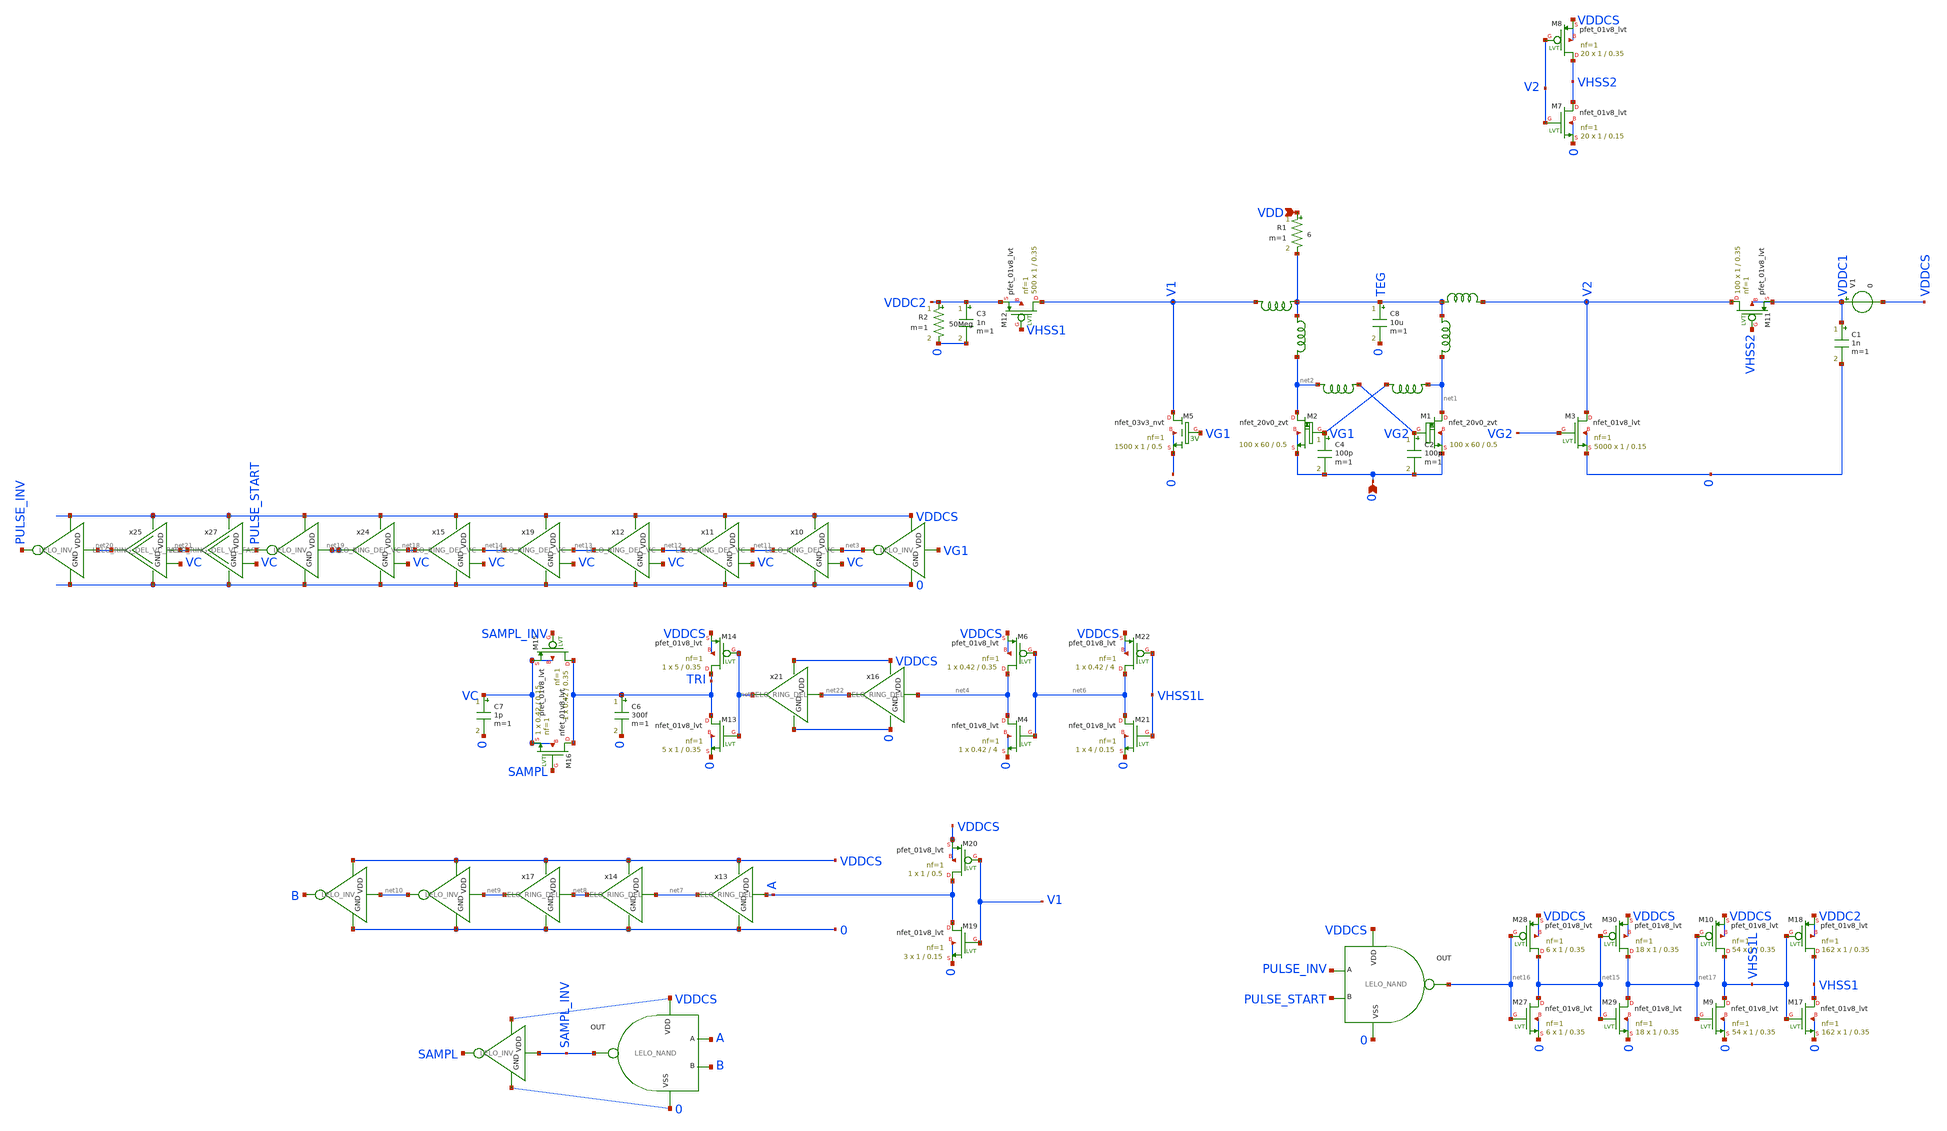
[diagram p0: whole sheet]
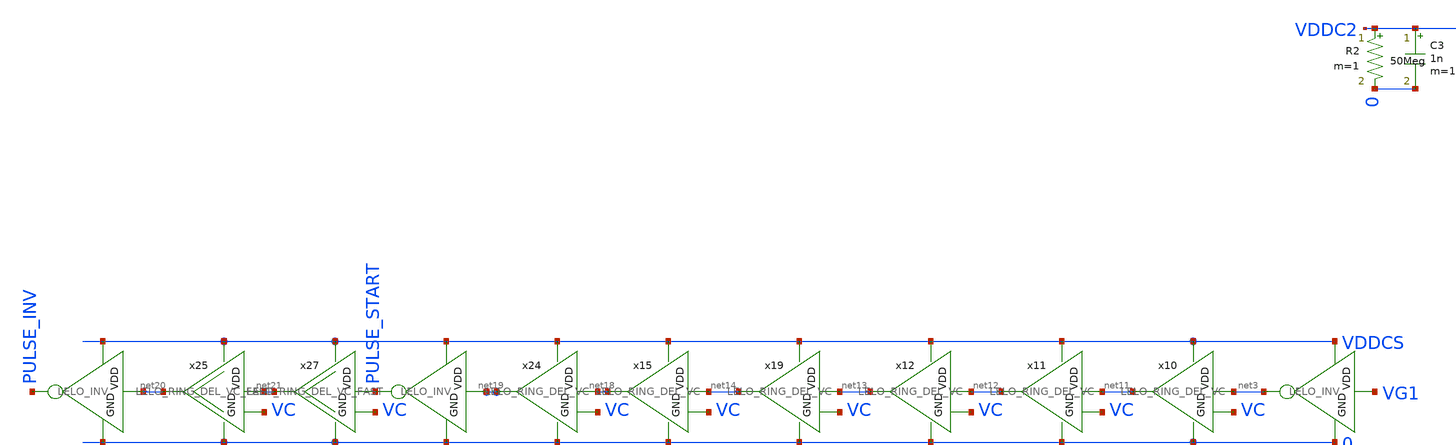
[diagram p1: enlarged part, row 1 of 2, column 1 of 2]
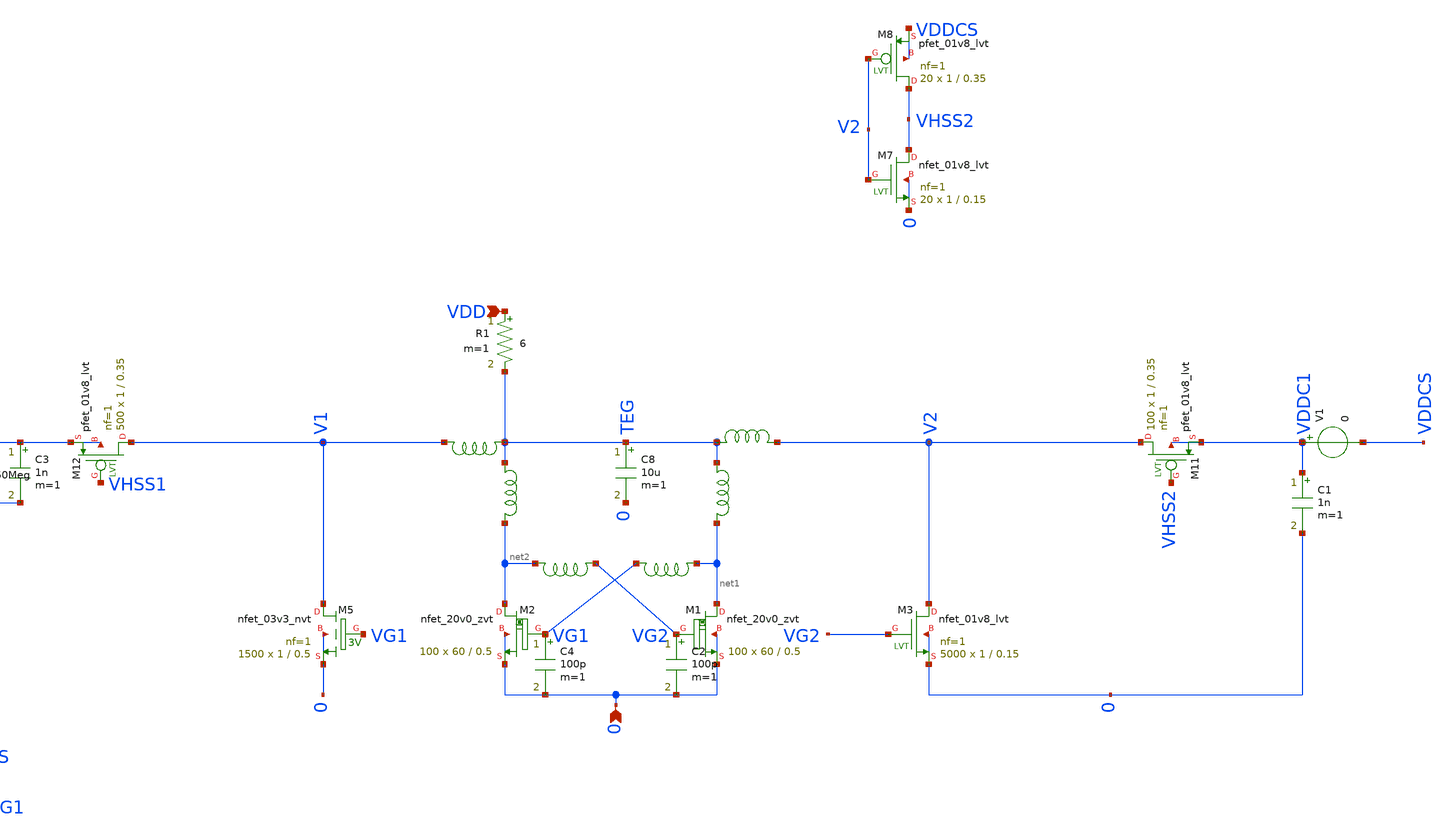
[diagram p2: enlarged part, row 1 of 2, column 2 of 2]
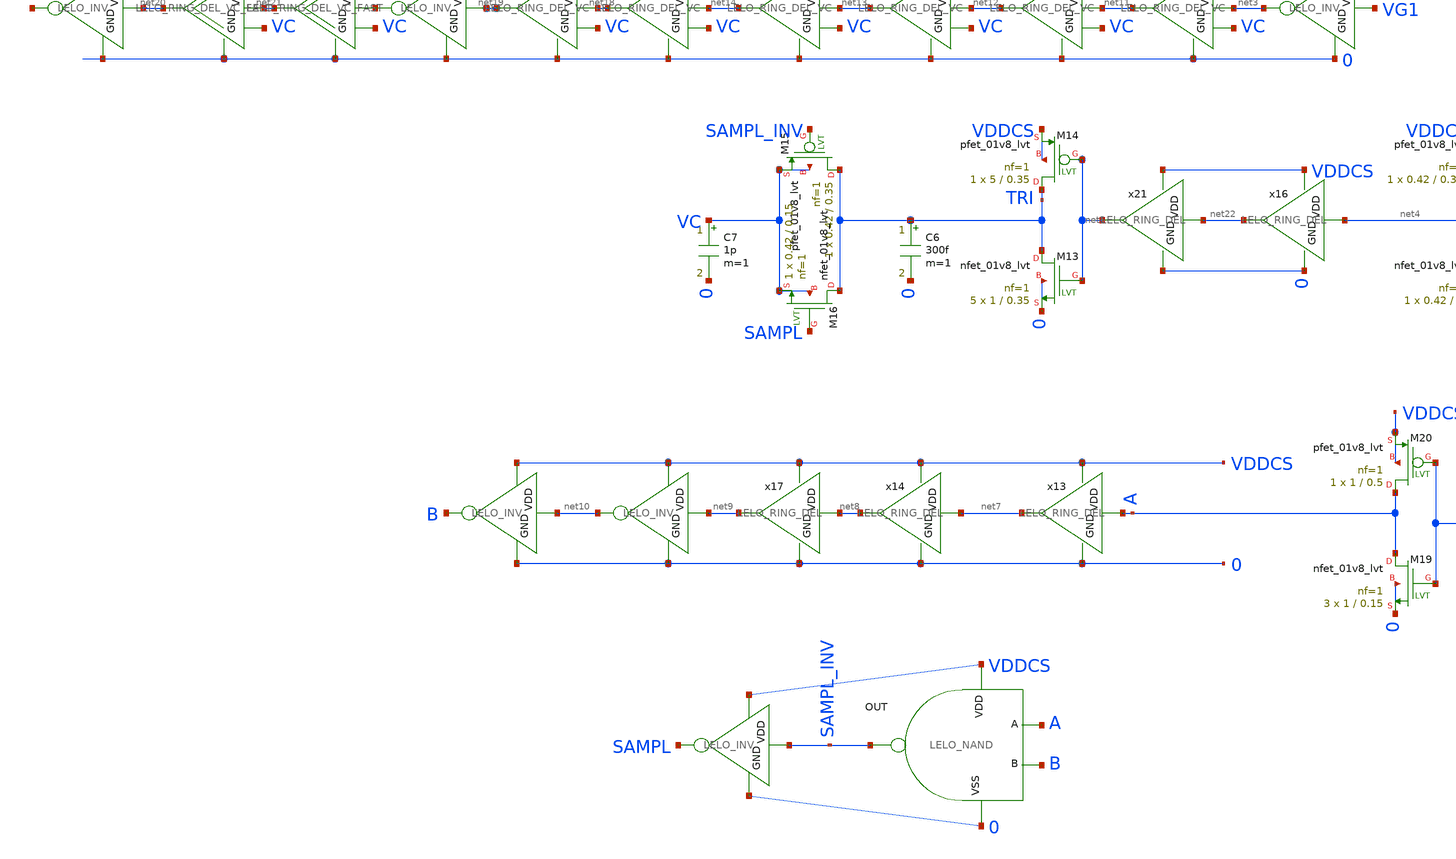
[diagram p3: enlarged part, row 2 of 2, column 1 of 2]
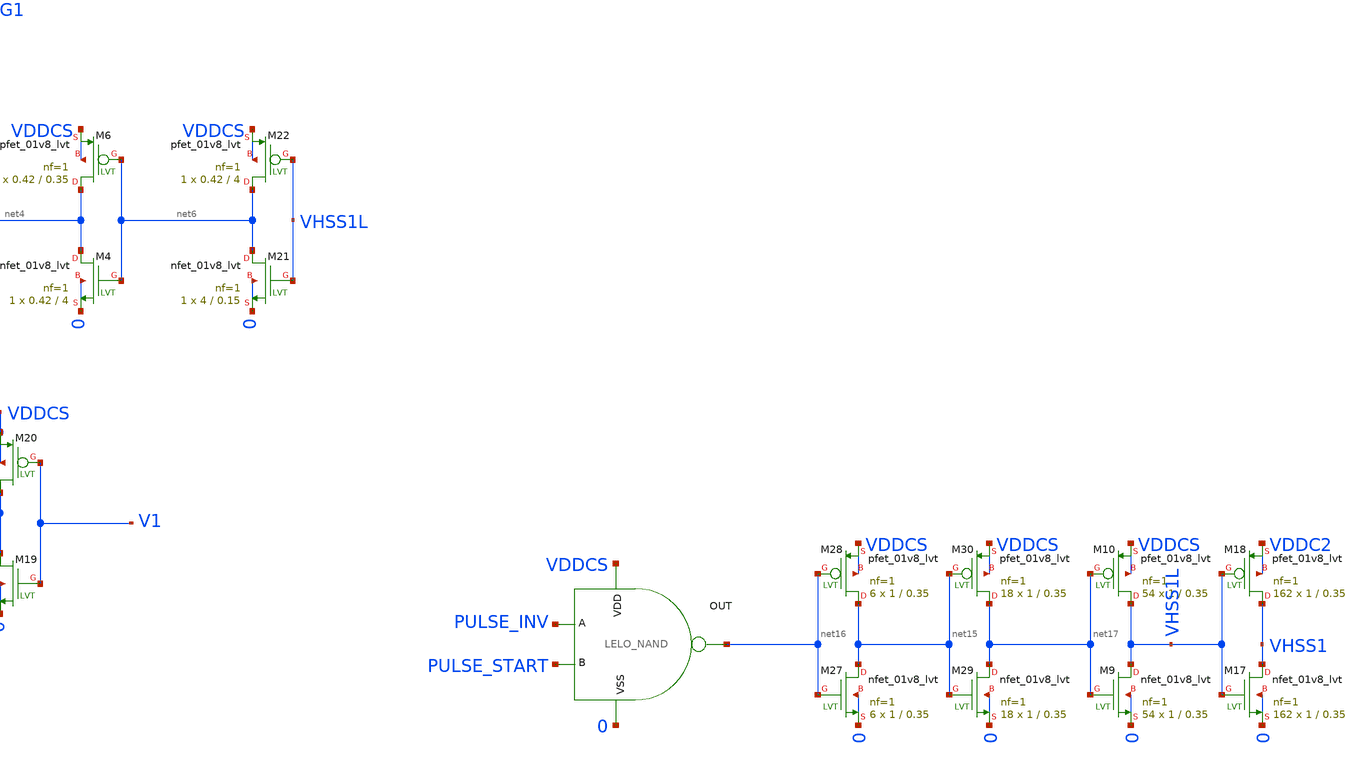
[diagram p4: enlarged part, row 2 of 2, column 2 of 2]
** sch_path: design/LELO_SVOD_SKY130A/LELO_EXSC.sch
**.subckt LELO_EXSC 0 VDD
*.ipin 0
*.ipin VDD
C1 VDDC1 0 1n m=1
C2 VG2 0 100p m=1
R1 VDD TEG 6 m=1
XM3 V2 VG2 0 0 sky130_fd_pr__nfet_01v8_lvt L=0.15 W=1 nf=1 ad='int((1 + 1)/2) * 1 / 1 * 0.29' as='int((1 + 2)/2) * 1 / 1 * 0.29'
+ pd='2*int((1 + 1)/2) * (1 / 1 + 0.29)' ps='2*int((1 + 2)/2) * (1 / 1 + 0.29)' nrd='0.29 / 1 ' nrs='0.29 / 1 '
+ sa=0 sb=0 sd=0 mult=5000 m=5000
x1 VG2 net2 1812PS-564_imp
x2 net1 VG1 1812PS-564_imp
C4 VG1 0 100p m=1
XM11 V2 VHSS2 VDDC1 VDDC1 sky130_fd_pr__pfet_01v8_lvt L=0.35 W=1 nf=1 ad='int((1 + 1)/2) * 1 / 1 * 0.29'
+ as='int((1 + 2)/2) * 1 / 1 * 0.29' pd='2*int((1 + 1)/2) * (1 / 1 + 0.29)' ps='2*int((1 + 2)/2) * (1 / 1 + 0.29)'
+ nrd='0.29 / 1 ' nrs='0.29 / 1 ' sa=0 sb=0 sd=0 mult=100 m=100
XM12 V1 VHSS1 VDDC2 VDDC2 sky130_fd_pr__pfet_01v8_lvt L=0.35 W=1 nf=1 ad='int((1 + 1)/2) * 1 / 1 * 0.29'
+ as='int((1 + 2)/2) * 1 / 1 * 0.29' pd='2*int((1 + 1)/2) * (1 / 1 + 0.29)' ps='2*int((1 + 2)/2) * (1 / 1 + 0.29)'
+ nrd='0.29 / 1 ' nrs='0.29 / 1 ' sa=0 sb=0 sd=0 mult=500 m=500
XM1 net1 VG2 0 0 sky130_fd_pr__nfet_20v0_zvt W=60 L=0.5 m=100
XM2 net2 VG1 0 0 sky130_fd_pr__nfet_20v0_zvt W=60 L=0.5 m=100
x9 VDDCS VG1 net3 0 LELO_INV
XM4 net4 net6 0 0 sky130_fd_pr__nfet_01v8_lvt L=4 W=0.42 nf=1 ad='int((1 + 1)/2) * 0.42 / 1 * 0.29' as='int((1 + 2)/2) * 0.42 / 1 * 0.29'
+ pd='2*int((1 + 1)/2) * (0.42 / 1 + 0.29)' ps='2*int((1 + 2)/2) * (0.42 / 1 + 0.29)' nrd='0.29 / 0.42 '
+ nrs='0.29 / 0.42 ' sa=0 sb=0 sd=0 mult=1 m=1
XM6 net4 net6 VDDCS VDDCS sky130_fd_pr__pfet_01v8_lvt L=0.35 W=0.42 nf=1 ad='int((1 + 1)/2) * 0.42 / 1 * 0.29'
+ as='int((1 + 2)/2) * 0.42 / 1 * 0.29' pd='2*int((1 + 1)/2) * (0.42 / 1 + 0.29)' ps='2*int((1 + 2)/2) * (0.42 / 1 + 0.29)'
+ nrd='0.29 / 0.42 ' nrs='0.29 / 0.42 ' sa=0 sb=0 sd=0 mult=1 m=1
XM13 TRI net5 0 0 sky130_fd_pr__nfet_01v8_lvt L=0.35 W=1 nf=1 ad='int((1 + 1)/2) * 1 / 1 * 0.29' as='int((1 + 2)/2) * 1 / 1 * 0.29'
+ pd='2*int((1 + 1)/2) * (1 / 1 + 0.29)' ps='2*int((1 + 2)/2) * (1 / 1 + 0.29)' nrd='0.29 / 1 ' nrs='0.29 / 1 '
+ sa=0 sb=0 sd=0 mult=5 m=5
XM14 TRI net5 VDDCS VDDCS sky130_fd_pr__pfet_01v8_lvt L=0.35 W=5 nf=1 ad='int((1 + 1)/2) * 5 / 1 * 0.29'
+ as='int((1 + 2)/2) * 5 / 1 * 0.29' pd='2*int((1 + 1)/2) * (5 / 1 + 0.29)' ps='2*int((1 + 2)/2) * (5 / 1 + 0.29)'
+ nrd='0.29 / 5 ' nrs='0.29 / 5 ' sa=0 sb=0 sd=0 mult=1 m=1
C6 TRI 0 300f m=1
C7 VC 0 1p m=1
XM15 TRI SAMPL_INV VC VC sky130_fd_pr__pfet_01v8_lvt L=0.35 W=0.42 nf=1 ad='int((1 + 1)/2) * 0.42 / 1 * 0.29'
+ as='int((1 + 2)/2) * 0.42 / 1 * 0.29' pd='2*int((1 + 1)/2) * (0.42 / 1 + 0.29)' ps='2*int((1 + 2)/2) * (0.42 / 1 + 0.29)'
+ nrd='0.29 / 0.42 ' nrs='0.29 / 0.42 ' sa=0 sb=0 sd=0 mult=1 m=1
XM16 TRI SAMPL VC VC sky130_fd_pr__nfet_01v8_lvt L=0.15 W=0.42 nf=1 ad='int((1 + 1)/2) * 0.42 / 1 * 0.29'
+ as='int((1 + 2)/2) * 0.42 / 1 * 0.29' pd='2*int((1 + 1)/2) * (0.42 / 1 + 0.29)' ps='2*int((1 + 2)/2) * (0.42 / 1 + 0.29)'
+ nrd='0.29 / 0.42 ' nrs='0.29 / 0.42 ' sa=0 sb=0 sd=0 mult=1 m=1
x13 VDDCS A net7 0 LELO_RING_DEL
x14 VDDCS net7 net8 0 LELO_RING_DEL
x10 VDDCS net3 net11 0 VC LELO_RING_DEL_VC
x11 VDDCS net11 net12 0 VC LELO_RING_DEL_VC
x12 VDDCS net12 net13 0 VC LELO_RING_DEL_VC
C8 TEG 0 10u m=1
x20 VDDCS SAMPL_INV A B 0 LELO_NAND
x17 VDDCS net8 net9 0 LELO_RING_DEL
x18 VDDCS net9 net10 0 LELO_INV
x22 VDDCS net10 B 0 LELO_INV
x23 VDDCS SAMPL_INV SAMPL 0 LELO_INV
x19 VDDCS net13 net14 0 VC LELO_RING_DEL_VC
XM19 A V1 0 0 sky130_fd_pr__nfet_01v8_lvt L=0.15 W=1 nf=1 ad='int((1 + 1)/2) * 1 / 1 * 0.29' as='int((1 + 2)/2) * 1 / 1 * 0.29'
+ pd='2*int((1 + 1)/2) * (1 / 1 + 0.29)' ps='2*int((1 + 2)/2) * (1 / 1 + 0.29)' nrd='0.29 / 1 ' nrs='0.29 / 1 '
+ sa=0 sb=0 sd=0 mult=3 m=3
XM20 A V1 VDDCS VDDCS sky130_fd_pr__pfet_01v8_lvt L=0.5 W=1 nf=1 ad='int((1 + 1)/2) * 1 / 1 * 0.29' as='int((1 + 2)/2) * 1 / 1 * 0.29'
+ pd='2*int((1 + 1)/2) * (1 / 1 + 0.29)' ps='2*int((1 + 2)/2) * (1 / 1 + 0.29)' nrd='0.29 / 1 ' nrs='0.29 / 1 '
+ sa=0 sb=0 sd=0 mult=1 m=1
XM7 VHSS2 V2 0 0 sky130_fd_pr__nfet_01v8_lvt L=0.15 W=1 nf=1 ad='int((1 + 1)/2) * 1 / 1 * 0.29' as='int((1 + 2)/2) * 1 / 1 * 0.29'
+ pd='2*int((1 + 1)/2) * (1 / 1 + 0.29)' ps='2*int((1 + 2)/2) * (1 / 1 + 0.29)' nrd='0.29 / 1 ' nrs='0.29 / 1 '
+ sa=0 sb=0 sd=0 mult=20 m=20
XM8 VHSS2 V2 VDDCS VDDCS sky130_fd_pr__pfet_01v8_lvt L=0.35 W=1 nf=1 ad='int((1 + 1)/2) * 1 / 1 * 0.29'
+ as='int((1 + 2)/2) * 1 / 1 * 0.29' pd='2*int((1 + 1)/2) * (1 / 1 + 0.29)' ps='2*int((1 + 2)/2) * (1 / 1 + 0.29)'
+ nrd='0.29 / 1 ' nrs='0.29 / 1 ' sa=0 sb=0 sd=0 mult=20 m=20
x8 VDDCS net16 PULSE_INV PULSE_START 0 LELO_NAND
XM27 net15 net16 0 0 sky130_fd_pr__nfet_01v8_lvt L=0.35 W=1 nf=1 ad='int((1 + 1)/2) * 1 / 1 * 0.29' as='int((1 + 2)/2) * 1 / 1 * 0.29'
+ pd='2*int((1 + 1)/2) * (1 / 1 + 0.29)' ps='2*int((1 + 2)/2) * (1 / 1 + 0.29)' nrd='0.29 / 1 ' nrs='0.29 / 1 '
+ sa=0 sb=0 sd=0 mult=6 m=6
XM28 net15 net16 VDDCS VDDCS sky130_fd_pr__pfet_01v8_lvt L=0.35 W=1 nf=1 ad='int((1 + 1)/2) * 1 / 1 * 0.29'
+ as='int((1 + 2)/2) * 1 / 1 * 0.29' pd='2*int((1 + 1)/2) * (1 / 1 + 0.29)' ps='2*int((1 + 2)/2) * (1 / 1 + 0.29)'
+ nrd='0.29 / 1 ' nrs='0.29 / 1 ' sa=0 sb=0 sd=0 mult=6 m=6
XM29 net17 net15 0 0 sky130_fd_pr__nfet_01v8_lvt L=0.35 W=1 nf=1 ad='int((1 + 1)/2) * 1 / 1 * 0.29' as='int((1 + 2)/2) * 1 / 1 * 0.29'
+ pd='2*int((1 + 1)/2) * (1 / 1 + 0.29)' ps='2*int((1 + 2)/2) * (1 / 1 + 0.29)' nrd='0.29 / 1 ' nrs='0.29 / 1 '
+ sa=0 sb=0 sd=0 mult=18 m=18
XM30 net17 net15 VDDCS VDDCS sky130_fd_pr__pfet_01v8_lvt L=0.35 W=1 nf=1 ad='int((1 + 1)/2) * 1 / 1 * 0.29'
+ as='int((1 + 2)/2) * 1 / 1 * 0.29' pd='2*int((1 + 1)/2) * (1 / 1 + 0.29)' ps='2*int((1 + 2)/2) * (1 / 1 + 0.29)'
+ nrd='0.29 / 1 ' nrs='0.29 / 1 ' sa=0 sb=0 sd=0 mult=18 m=18
x3 TEG net2 1812PS-103_imp
x4 TEG net1 1812PS-103_imp
x5 TEG V2 XGL6030-822_sat
x25 VDDCS net21 net20 0 VC LELO_RING_DEL_VC_FAST
x6 VDDCS net20 PULSE_INV 0 LELO_INV
x15 VDDCS net14 net18 0 VC LELO_RING_DEL_VC
C3 VDDC2 0 1n m=1
R2 VDDC2 0 50Meg m=1
V1 VDDC1 VDDCS 0
.save i(v1)
XM9 VHSS1L net17 0 0 sky130_fd_pr__nfet_01v8_lvt L=0.35 W=1 nf=1 ad='int((1 + 1)/2) * 1 / 1 * 0.29' as='int((1 + 2)/2) * 1 / 1 * 0.29'
+ pd='2*int((1 + 1)/2) * (1 / 1 + 0.29)' ps='2*int((1 + 2)/2) * (1 / 1 + 0.29)' nrd='0.29 / 1 ' nrs='0.29 / 1 '
+ sa=0 sb=0 sd=0 mult=54 m=54
XM10 VHSS1L net17 VDDCS VDDCS sky130_fd_pr__pfet_01v8_lvt L=0.35 W=1 nf=1 ad='int((1 + 1)/2) * 1 / 1 * 0.29'
+ as='int((1 + 2)/2) * 1 / 1 * 0.29' pd='2*int((1 + 1)/2) * (1 / 1 + 0.29)' ps='2*int((1 + 2)/2) * (1 / 1 + 0.29)'
+ nrd='0.29 / 1 ' nrs='0.29 / 1 ' sa=0 sb=0 sd=0 mult=54 m=54
XM17 VHSS1 VHSS1L 0 0 sky130_fd_pr__nfet_01v8_lvt L=0.35 W=1 nf=1 ad='int((1 + 1)/2) * 1 / 1 * 0.29'
+ as='int((1 + 2)/2) * 1 / 1 * 0.29' pd='2*int((1 + 1)/2) * (1 / 1 + 0.29)' ps='2*int((1 + 2)/2) * (1 / 1 + 0.29)'
+ nrd='0.29 / 1 ' nrs='0.29 / 1 ' sa=0 sb=0 sd=0 mult=162 m=162
XM18 VHSS1 VHSS1L VDDC2 VDDC2 sky130_fd_pr__pfet_01v8_lvt L=0.35 W=1 nf=1 ad='int((1 + 1)/2) * 1 / 1 * 0.29'
+ as='int((1 + 2)/2) * 1 / 1 * 0.29' pd='2*int((1 + 1)/2) * (1 / 1 + 0.29)' ps='2*int((1 + 2)/2) * (1 / 1 + 0.29)'
+ nrd='0.29 / 1 ' nrs='0.29 / 1 ' sa=0 sb=0 sd=0 mult=162 m=162
x7 TEG V1 XGL6030-822_sat
x26 VDDCS net19 PULSE_START 0 LELO_INV
x27 VDDCS PULSE_START net21 0 VC LELO_RING_DEL_VC_FAST
x24 VDDCS net18 net19 0 VC LELO_RING_DEL_VC
XM21 net6 VHSS1L 0 0 sky130_fd_pr__nfet_01v8_lvt L=0.15 W=4 nf=1 ad='int((1 + 1)/2) * 4 / 1 * 0.29' as='int((1 + 2)/2) * 4 / 1 * 0.29'
+ pd='2*int((1 + 1)/2) * (4 / 1 + 0.29)' ps='2*int((1 + 2)/2) * (4 / 1 + 0.29)' nrd='0.29 / 4 ' nrs='0.29 / 4 '
+ sa=0 sb=0 sd=0 mult=1 m=1
XM22 net6 VHSS1L VDDCS VDDCS sky130_fd_pr__pfet_01v8_lvt L=4 W=0.42 nf=1 ad='int((1 + 1)/2) * 0.42 / 1 * 0.29'
+ as='int((1 + 2)/2) * 0.42 / 1 * 0.29' pd='2*int((1 + 1)/2) * (0.42 / 1 + 0.29)' ps='2*int((1 + 2)/2) * (0.42 / 1 + 0.29)'
+ nrd='0.29 / 0.42 ' nrs='0.29 / 0.42 ' sa=0 sb=0 sd=0 mult=1 m=1
x16 VDDCS net4 net22 0 LELO_RING_DEL
x21 VDDCS net22 net5 0 LELO_RING_DEL
XM5 V1 VG1 0 0 sky130_fd_pr__nfet_03v3_nvt L=0.5 W=1 nf=1 ad='int((1 + 1)/2) * 1 / 1 * 0.29' as='int((1 + 2)/2) * 1 / 1 * 0.29'
+ pd='2*int((1 + 1)/2) * (1 / 1 + 0.29)' ps='2*int((1 + 2)/2) * (1 / 1 + 0.29)' nrd='0.29 / 1 ' nrs='0.29 / 1 '
+ sa=0 sb=0 sd=0 mult=1500 m=1500
**.ends

* expanding   symbol:  LELO_SVOD_SKY130A/1812PS-564_imp.sym # of pins=2
** sym_path: design/LELO_SVOD_SKY130A/1812PS-564_imp.sym

.subckt 1812PS-564_imp port1 port2
X1 port1 port2 Model1D R1=70 R2=6.1 C= 7.71p K1=0.000001 K2=115.8 K3= 560u K4=0.000001 K5=0.000001
+ L=0 Is=0 a=0 L_Z0=0 L_EL=0 L_F0=0E6 PkZ=153558.837
.ends 1812PS-564_imp

* expanding   symbol:  LELO_SVOD_SKY130A/LELO_INV.sym # of pins=4
** sym_path: design/LELO_SVOD_SKY130A/LELO_INV.sym
** sch_path: design/LELO_SVOD_SKY130A/LELO_INV.sch
.subckt LELO_INV VDD VIN VOUT GND
*.ipin VIN
*.ipin VDD
*.ipin GND
*.opin VOUT
XM1 VOUT VIN GND GND sky130_fd_pr__nfet_01v8_lvt L=0.15 W=1 nf=1 ad='int((1 + 1)/2) * 1 / 1 * 0.29' as='int((1 + 2)/2) * 1 / 1 * 0.29'
+ pd='2*int((1 + 1)/2) * (1 / 1 + 0.29)' ps='2*int((1 + 2)/2) * (1 / 1 + 0.29)' nrd='0.29 / 1 ' nrs='0.29 / 1 '
+ sa=0 sb=0 sd=0 mult=1 m=1
XM2 VOUT VIN VDD VDD sky130_fd_pr__pfet_01v8_lvt L=0.35 W=1 nf=1 ad='int((1 + 1)/2) * 1 / 1 * 0.29' as='int((1 + 2)/2) * 1 / 1 * 0.29'
+ pd='2*int((1 + 1)/2) * (1 / 1 + 0.29)' ps='2*int((1 + 2)/2) * (1 / 1 + 0.29)' nrd='0.29 / 1 ' nrs='0.29 / 1 '
+ sa=0 sb=0 sd=0 mult=2 m=2
.ends


* expanding   symbol:  LELO_SVOD_SKY130A/LELO_RING_DEL.sym # of pins=4
** sym_path: design/LELO_SVOD_SKY130A/LELO_RING_DEL.sym
** sch_path: design/LELO_SVOD_SKY130A/LELO_RING_DEL.sch
.subckt LELO_RING_DEL VDD VIN VOUT GND
*.ipin VIN
*.ipin VDD
*.ipin GND
*.opin VOUT
XM1 VOUT VIN GND GND sky130_fd_pr__nfet_01v8_lvt L=1 W=0.42 nf=1 ad='int((1 + 1)/2) * 0.42 / 1 * 0.29'
+ as='int((1 + 2)/2) * 0.42 / 1 * 0.29' pd='2*int((1 + 1)/2) * (0.42 / 1 + 0.29)' ps='2*int((1 + 2)/2) * (0.42 / 1 + 0.29)'
+ nrd='0.29 / 0.42 ' nrs='0.29 / 0.42 ' sa=0 sb=0 sd=0 mult=1 m=1
XM2 VOUT VIN VDD VDD sky130_fd_pr__pfet_01v8_lvt L=1 W=0.42 nf=1 ad='int((1 + 1)/2) * 0.42 / 1 * 0.29'
+ as='int((1 + 2)/2) * 0.42 / 1 * 0.29' pd='2*int((1 + 1)/2) * (0.42 / 1 + 0.29)' ps='2*int((1 + 2)/2) * (0.42 / 1 + 0.29)'
+ nrd='0.29 / 0.42 ' nrs='0.29 / 0.42 ' sa=0 sb=0 sd=0 mult=1 m=1
.ends


* expanding   symbol:  LELO_SVOD_SKY130A/LELO_RING_DEL_VC.sym # of pins=5
** sym_path: design/LELO_SVOD_SKY130A/LELO_RING_DEL_VC.sym
** sch_path: design/LELO_SVOD_SKY130A/LELO_RING_DEL_VC.sch
.subckt LELO_RING_DEL_VC VDD VIN VOUT GND VC
*.ipin VIN
*.ipin VDD
*.ipin GND
*.opin VOUT
*.ipin VC
XM1 VOUT VIN net1 GND sky130_fd_pr__nfet_01v8_lvt L=0.15 W=0.42 nf=1 ad='int((1 + 1)/2) * 0.42 / 1 * 0.29'
+ as='int((1 + 2)/2) * 0.42 / 1 * 0.29' pd='2*int((1 + 1)/2) * (0.42 / 1 + 0.29)' ps='2*int((1 + 2)/2) * (0.42 / 1 + 0.29)'
+ nrd='0.29 / 0.42 ' nrs='0.29 / 0.42 ' sa=0 sb=0 sd=0 mult=1 m=1
XM2 VOUT VIN VDD VDD sky130_fd_pr__pfet_01v8_lvt L=3 W=0.42 nf=1 ad='int((1 + 1)/2) * 0.42 / 1 * 0.29'
+ as='int((1 + 2)/2) * 0.42 / 1 * 0.29' pd='2*int((1 + 1)/2) * (0.42 / 1 + 0.29)' ps='2*int((1 + 2)/2) * (0.42 / 1 + 0.29)'
+ nrd='0.29 / 0.42 ' nrs='0.29 / 0.42 ' sa=0 sb=0 sd=0 mult=1 m=1
XM3 net1 VIN GND GND sky130_fd_pr__nfet_01v8_lvt L=4 W=0.42 nf=1 ad='int((1 + 1)/2) * 0.42 / 1 * 0.29'
+ as='int((1 + 2)/2) * 0.42 / 1 * 0.29' pd='2*int((1 + 1)/2) * (0.42 / 1 + 0.29)' ps='2*int((1 + 2)/2) * (0.42 / 1 + 0.29)'
+ nrd='0.29 / 0.42 ' nrs='0.29 / 0.42 ' sa=0 sb=0 sd=0 mult=1 m=1
XM4 net1 VC GND GND sky130_fd_pr__nfet_01v8_lvt L=4 W=0.42 nf=1 ad='int((1 + 1)/2) * 0.42 / 1 * 0.29'
+ as='int((1 + 2)/2) * 0.42 / 1 * 0.29' pd='2*int((1 + 1)/2) * (0.42 / 1 + 0.29)' ps='2*int((1 + 2)/2) * (0.42 / 1 + 0.29)'
+ nrd='0.29 / 0.42 ' nrs='0.29 / 0.42 ' sa=0 sb=0 sd=0 mult=1 m=1
.ends


* expanding   symbol:  LELO_SVOD_SKY130A/LELO_NAND.sym # of pins=5
** sym_path: design/LELO_SVOD_SKY130A/LELO_NAND.sym
** sch_path: design/LELO_SVOD_SKY130A/LELO_NAND.sch
.subckt LELO_NAND VDD OUT A B VSS
*.ipin VDD
*.ipin VSS
*.opin OUT
*.ipin A
*.ipin B
XM1 OUT B net1 net1 sky130_fd_pr__nfet_01v8_lvt L=0.15 W=5 nf=1 ad='int((1 + 1)/2) * 5 / 1 * 0.29' as='int((1 + 2)/2) * 5 / 1 * 0.29'
+ pd='2*int((1 + 1)/2) * (5 / 1 + 0.29)' ps='2*int((1 + 2)/2) * (5 / 1 + 0.29)' nrd='0.29 / 5 ' nrs='0.29 / 5 '
+ sa=0 sb=0 sd=0 mult=1 m=1
XM2 net1 A VSS VSS sky130_fd_pr__nfet_01v8_lvt L=0.15 W=5 nf=1 ad='int((1 + 1)/2) * 5 / 1 * 0.29' as='int((1 + 2)/2) * 5 / 1 * 0.29'
+ pd='2*int((1 + 1)/2) * (5 / 1 + 0.29)' ps='2*int((1 + 2)/2) * (5 / 1 + 0.29)' nrd='0.29 / 5 ' nrs='0.29 / 5 '
+ sa=0 sb=0 sd=0 mult=1 m=1
XM3 OUT A VDD VDD sky130_fd_pr__pfet_01v8_lvt L=0.35 W=1 nf=1 ad='int((1 + 1)/2) * 1 / 1 * 0.29' as='int((1 + 2)/2) * 1 / 1 * 0.29'
+ pd='2*int((1 + 1)/2) * (1 / 1 + 0.29)' ps='2*int((1 + 2)/2) * (1 / 1 + 0.29)' nrd='0.29 / 1 ' nrs='0.29 / 1 '
+ sa=0 sb=0 sd=0 mult=1 m=1
XM4 OUT B VDD net2 sky130_fd_pr__pfet_01v8_lvt L=0.35 W=1 nf=1 ad='int((1 + 1)/2) * 1 / 1 * 0.29' as='int((1 + 2)/2) * 1 / 1 * 0.29'
+ pd='2*int((1 + 1)/2) * (1 / 1 + 0.29)' ps='2*int((1 + 2)/2) * (1 / 1 + 0.29)' nrd='0.29 / 1 ' nrs='0.29 / 1 '
+ sa=0 sb=0 sd=0 mult=1 m=1
.ends


* expanding   symbol:  LELO_SVOD_SKY130A/1812PS-103_imp.sym # of pins=2
** sym_path: design/LELO_SVOD_SKY130A/1812PS-103_imp.sym

.subckt 1812PS-103_imp port1 port2
X1 port1 port2 Model1D R1=29 R2=0.17 C= 0.28p K1=0.000001 K2=0.741 K3= 10u K4=0.0014 K5=0.0000509
+ L=0 Is=0 a=0 L_Z0=0 L_EL=0 L_F0=0E6 PkZ=7186.74953
.ends 1812PS-103_imp

* expanding   symbol:  LELO_SVOD_SKY130A/XGL6030-822_sat.sym # of pins=2
** sym_path: design/LELO_SVOD_SKY130A/XGL6030-822_sat.sym

.subckt XGL6030-822_sat port1 port2
X1 port1 port2 Model1C R1=5 R2=0.04 C= 15.2p K1=0.000001 K2=2 K3= 8.2u K4=0.000001 K5=0.000001
+ L=8.1093E-06 Is=13.9236 a=0.7109 L_Z0=0 L_EL=0 L_F0=0E6 PkZ=7057.14402
.ends XGL6030-822_sat


* expanding   symbol:  LELO_SVOD_SKY130A/LELO_RING_DEL_VC_FAST.sym # of pins=5
** sym_path: design/LELO_SVOD_SKY130A/LELO_RING_DEL_VC_FAST.sym
** sch_path: design/LELO_SVOD_SKY130A/LELO_RING_DEL_VC_FAST.sch
.subckt LELO_RING_DEL_VC_FAST VDD VIN VOUT GND VC
*.ipin VIN
*.ipin VDD
*.ipin GND
*.opin VOUT
*.ipin VC
XM1 VOUT VIN net1 GND sky130_fd_pr__nfet_01v8_lvt L=0.15 W=0.42 nf=1 ad='int((1 + 1)/2) * 0.42 / 1 * 0.29'
+ as='int((1 + 2)/2) * 0.42 / 1 * 0.29' pd='2*int((1 + 1)/2) * (0.42 / 1 + 0.29)' ps='2*int((1 + 2)/2) * (0.42 / 1 + 0.29)'
+ nrd='0.29 / 0.42 ' nrs='0.29 / 0.42 ' sa=0 sb=0 sd=0 mult=1 m=1
XM2 VOUT VIN VDD VDD sky130_fd_pr__pfet_01v8_lvt L=0.35 W=0.42 nf=1 ad='int((1 + 1)/2) * 0.42 / 1 * 0.29'
+ as='int((1 + 2)/2) * 0.42 / 1 * 0.29' pd='2*int((1 + 1)/2) * (0.42 / 1 + 0.29)' ps='2*int((1 + 2)/2) * (0.42 / 1 + 0.29)'
+ nrd='0.29 / 0.42 ' nrs='0.29 / 0.42 ' sa=0 sb=0 sd=0 mult=1 m=1
XM3 net1 VIN GND GND sky130_fd_pr__nfet_01v8_lvt L=0.35 W=0.42 nf=1 ad='int((1 + 1)/2) * 0.42 / 1 * 0.29'
+ as='int((1 + 2)/2) * 0.42 / 1 * 0.29' pd='2*int((1 + 1)/2) * (0.42 / 1 + 0.29)' ps='2*int((1 + 2)/2) * (0.42 / 1 + 0.29)'
+ nrd='0.29 / 0.42 ' nrs='0.29 / 0.42 ' sa=0 sb=0 sd=0 mult=1 m=1
XM4 net1 VC GND GND sky130_fd_pr__nfet_01v8_lvt L=0.35 W=4 nf=1 ad='int((1 + 1)/2) * 4 / 1 * 0.29' as='int((1 + 2)/2) * 4 / 1 * 0.29'
+ pd='2*int((1 + 1)/2) * (4 / 1 + 0.29)' ps='2*int((1 + 2)/2) * (4 / 1 + 0.29)' nrd='0.29 / 4 ' nrs='0.29 / 4 '
+ sa=0 sb=0 sd=0 mult=1 m=1
.ends

.end
